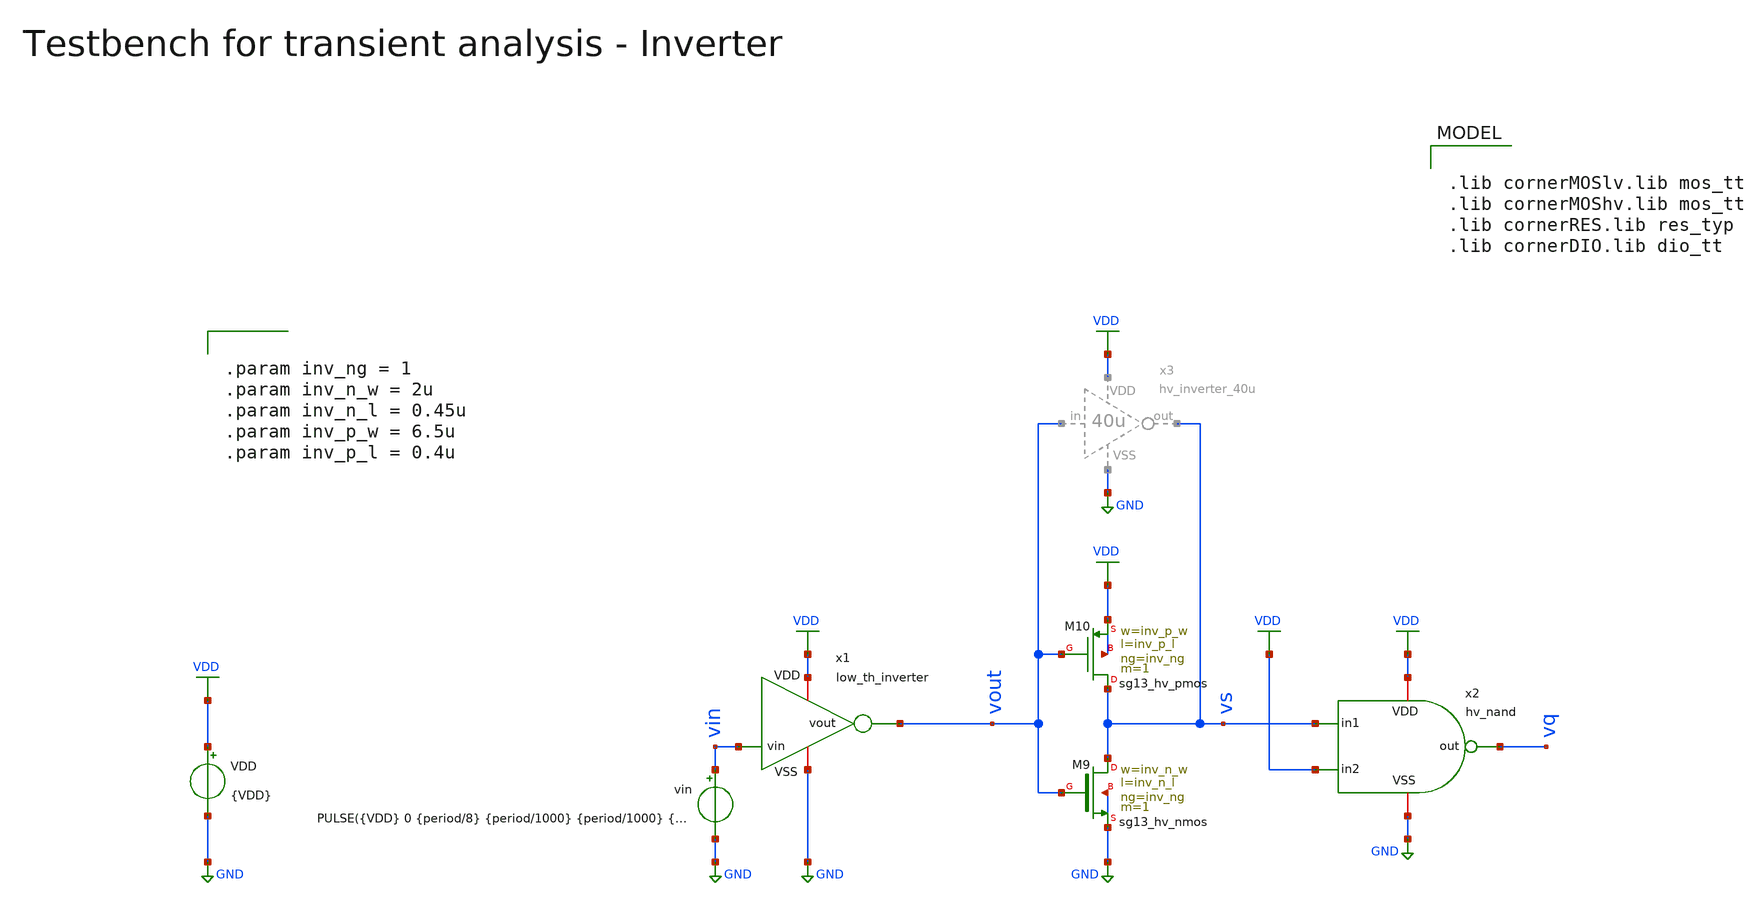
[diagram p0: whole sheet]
** sch_path: macros/heichips26_vcr/macros/switched_capacitor/testbenches/xschem/tb_lth_inv_tran.sch
**.subckt tb_lth_inv_tran
VDD VDD GND {VDD}
XM9 vs vout GND GND sg13_hv_nmos w=inv_n_w l=inv_n_l ng=inv_ng m=1 mm_ok=1
XM10 vs vout VDD VDD sg13_hv_pmos w=inv_p_w l=inv_p_l ng=inv_ng m=1 mm_ok=1
x2 VDD vs vq VDD GND hv_nand
vin vin GND PULSE({VDD} 0 {period/8} {period/1000} {period/1000} {period/2} {period})
x1 VDD vin vout GND low_th_inverter
**** begin user architecture code


.param VDD=3.3
.csparam VDD=VDD
.param Vcm=VDD/2
.param temp=27
.param Cload=10p
.param Rload=1k

.param period = 2n
.csparam tstop  = {1*period}
.csparam tstep  = {period/100}

.param vth = 1.65
.param vpp = {period*2.65e+6}
.param vmax = {vth+vpp/2}
.param vmin = {vth-vpp/2}

.ic v(vq) = 0

.options savecurrents klu method=gear reltol=1e-4 abstol=1e-15 gmin=1e-15
.control

save all

* Operating Point Analysis
op
remzerovec
write @schname\.raw
set appendwrite

* Transient Analysis
tran {$&tstep} {$&tstop}
write @schname\.raw

* Plotting
plot vin+4 vout vs vq+4
*plot vin1+4 50*(vin2-vin1)+4+vin1 vout vq+4
*plot vin1+4 vin2+4 vq+4 vout

* Write Data
unset appendwrite
set wr_vecnames
set wr_singlescale
*wrdata ../plot_simulations/data/@schname\.txt v(vin1) v(vin2) v(vout)

*quit
.endc



.lib cornerMOSlv.lib mos_tt
.lib cornerMOShv.lib mos_tt
.lib cornerRES.lib res_typ
.lib cornerDIO.lib dio_tt



.param inv_ng = 1
.param inv_n_w = 2u
.param inv_n_l = 0.45u
.param inv_p_w = 6.5u
.param inv_p_l = 0.4u


**** end user architecture code
**.ends

* expanding   symbol:  hv_inverter_40u.sym # of pins=4
** sym_path: macros/heichips26_vcr/macros/switched_capacitor/schematic/xschem/hv_inverter_40u.sym
** sch_path: macros/heichips26_vcr/macros/switched_capacitor/schematic/xschem/hv_inverter_40u.sch
.subckt hv_inverter_40u VDD in out VSS
*.ipin in
*.iopin VDD
*.iopin VSS
*.opin out
XM2 out in VSS VSS sg13_hv_nmos w={n_w} l={n_l} ng={ng} m=1 mm_ok=1
XM3 out in VDD VDD sg13_hv_pmos w={p_w} l={p_l} ng={ng} m=1 mm_ok=1
**** begin user architecture code


.param w   = 10u
.param ng  = 4
.param n_ng = ng
.param n_w = {3u*n_ng}
.param n_l = 0.45u
.param p_ng = ng
.param p_w = {10u*p_ng}
.param p_l = 0.4u


**** end user architecture code
.ends


* expanding   symbol:  hv_nand.sym # of pins=5
** sym_path: macros/heichips26_vcr/macros/switched_capacitor/schematic/xschem/hv_nand.sym
** sch_path: macros/heichips26_vcr/macros/switched_capacitor/schematic/xschem/hv_nand.sch
.subckt hv_nand VDD in1 out in2 VSS
*.ipin in1
*.iopin VDD
*.iopin VSS
*.opin out
*.ipin in2
**** begin user architecture code


.param w   = 10u
.param ng  = 4
.param n_ng = ng
.param n_w = {3u*n_ng}
.param n_l = 0.45u
.param p_ng = ng
.param p_w = {10u*p_ng}
.param p_l = 0.4u


**** end user architecture code
XM2 out in1 net1 VSS sg13_hv_nmos w={n_w} l={n_l} ng={ng} m=1 mm_ok=1
XM3 out in2 VDD VDD sg13_hv_pmos w={p_w} l={p_l} ng={ng} m=1 mm_ok=1
XM1 net1 in2 VSS VSS sg13_hv_nmos w={n_w} l={n_l} ng={ng} m=1 mm_ok=1
XM4 out in1 VDD VDD sg13_hv_pmos w={p_w} l={p_l} ng={ng} m=1 mm_ok=1
.ends


* expanding   symbol:  low_th_inverter.sym # of pins=4
** sym_path: macros/heichips26_vcr/macros/switched_capacitor/schematic/xschem/low_th_inverter.sym
** sch_path: macros/heichips26_vcr/macros/switched_capacitor/schematic/xschem/low_th_inverter.sch
.subckt low_th_inverter VDD vin vout VSS
*.ipin vin
*.iopin VDD
*.iopin VSS
*.opin vout
XM1 vout vin VSS VSS sg13_hv_nmos w={n_ng*n_w} l={n_l} ng={n_ng} m=1 mm_ok=1
XM2 vout vin VDD VDD sg13_hv_pmos w={p_ng*p_w} l={p_l} ng={n_ng} m=1 mm_ok=1
**** begin user architecture code


.param n_ng = 2
.param n_w = 1u
.param n_l = 0.45u
.param p_ng = 2
.param p_w = 1u
.param p_l = 0.4u


**** end user architecture code
.ends

.GLOBAL GND
.GLOBAL VDD
.end
